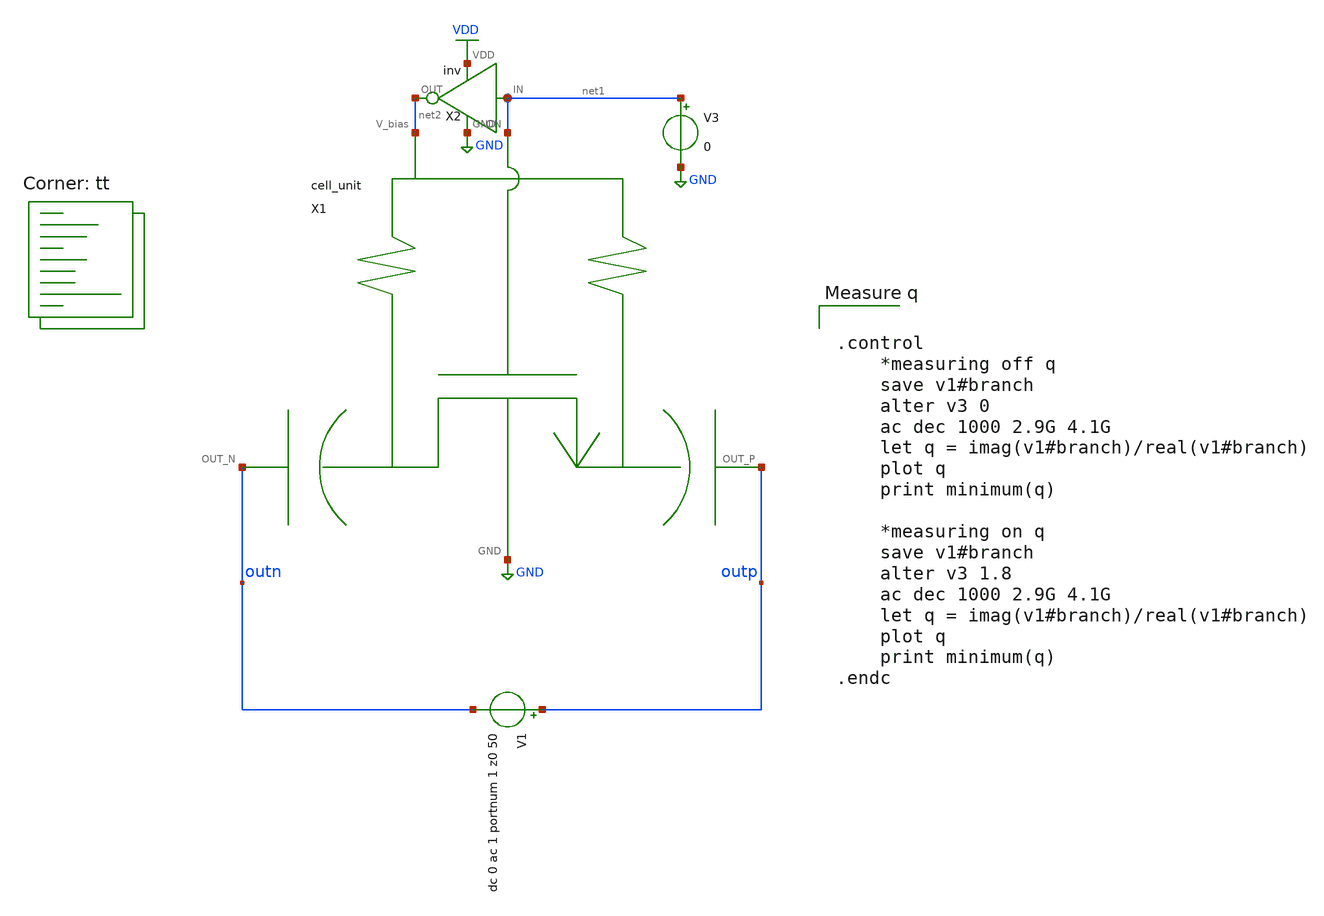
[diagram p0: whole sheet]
** sch_path: xschem/vco/testbenches/capbank/cell_unit_Q_measurement_tb.sch
**.subckt cell_unit_Q_measurement_tb
X1 net2 net1 outn GND outp cell_unit
X2 net1 net2 VDD GND inv
V3 net1 GND 0
V1 outp outn dc 0 ac 1 portnum 1 z0 50
**** begin user architecture code
.lib $::SKYWATER_MODELS/sky130.lib.spice tt


.control
    *measuring off q
    save v1#branch
    alter v3 0
    ac dec 1000 2.9G 4.1G
    let q = imag(v1#branch)/real(v1#branch)
    plot q
    print minimum(q)

    *measuring on q
    save v1#branch
    alter v3 1.8
    ac dec 1000 2.9G 4.1G
    let q = imag(v1#branch)/real(v1#branch)
    plot q
    print minimum(q)
.endc


**** end user architecture code
**.ends
.GLOBAL GND
.GLOBAL VDD
.end
